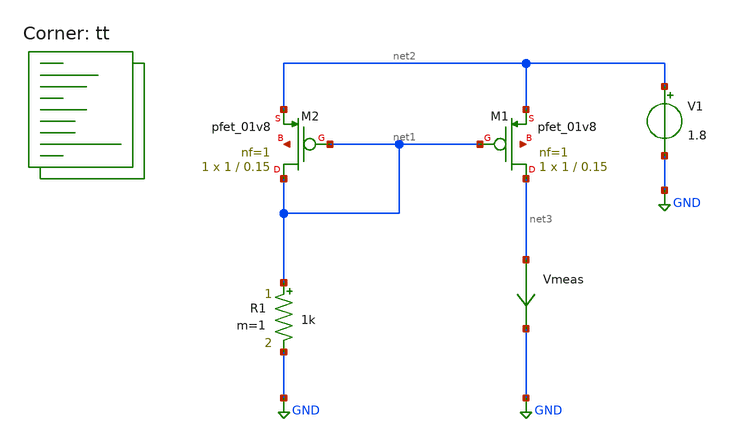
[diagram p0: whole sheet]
** sch_path: xschem/untitled.sch
**.subckt untitled
XM1 net3 net1 net2 net4 sky130_fd_pr__pfet_01v8 L=0.15 W=1 nf=1 ad='int((nf+1)/2) * W/nf * 0.29' as='int((nf+2)/2) * W/nf * 0.29'
+ pd='2*int((nf+1)/2) * (W/nf + 0.29)' ps='2*int((nf+2)/2) * (W/nf + 0.29)' nrd='0.29 / W' nrs='0.29 / W'
+ sa=0 sb=0 sd=0 mult=1 m=1
XM2 net1 net1 net2 net5 sky130_fd_pr__pfet_01v8 L=0.15 W=1 nf=1 ad='int((nf+1)/2) * W/nf * 0.29' as='int((nf+2)/2) * W/nf * 0.29'
+ pd='2*int((nf+1)/2) * (W/nf + 0.29)' ps='2*int((nf+2)/2) * (W/nf + 0.29)' nrd='0.29 / W' nrs='0.29 / W'
+ sa=0 sb=0 sd=0 mult=1 m=1
R1 net1 GND 1k m=1
Vmeas net3 GND 0
.save i(vmeas)
V1 net2 GND 1.8
**** begin user architecture code
.lib $::SKYWATER_MODELS/sky130.lib.spice tt
**** end user architecture code
**.ends
.GLOBAL GND
.end
